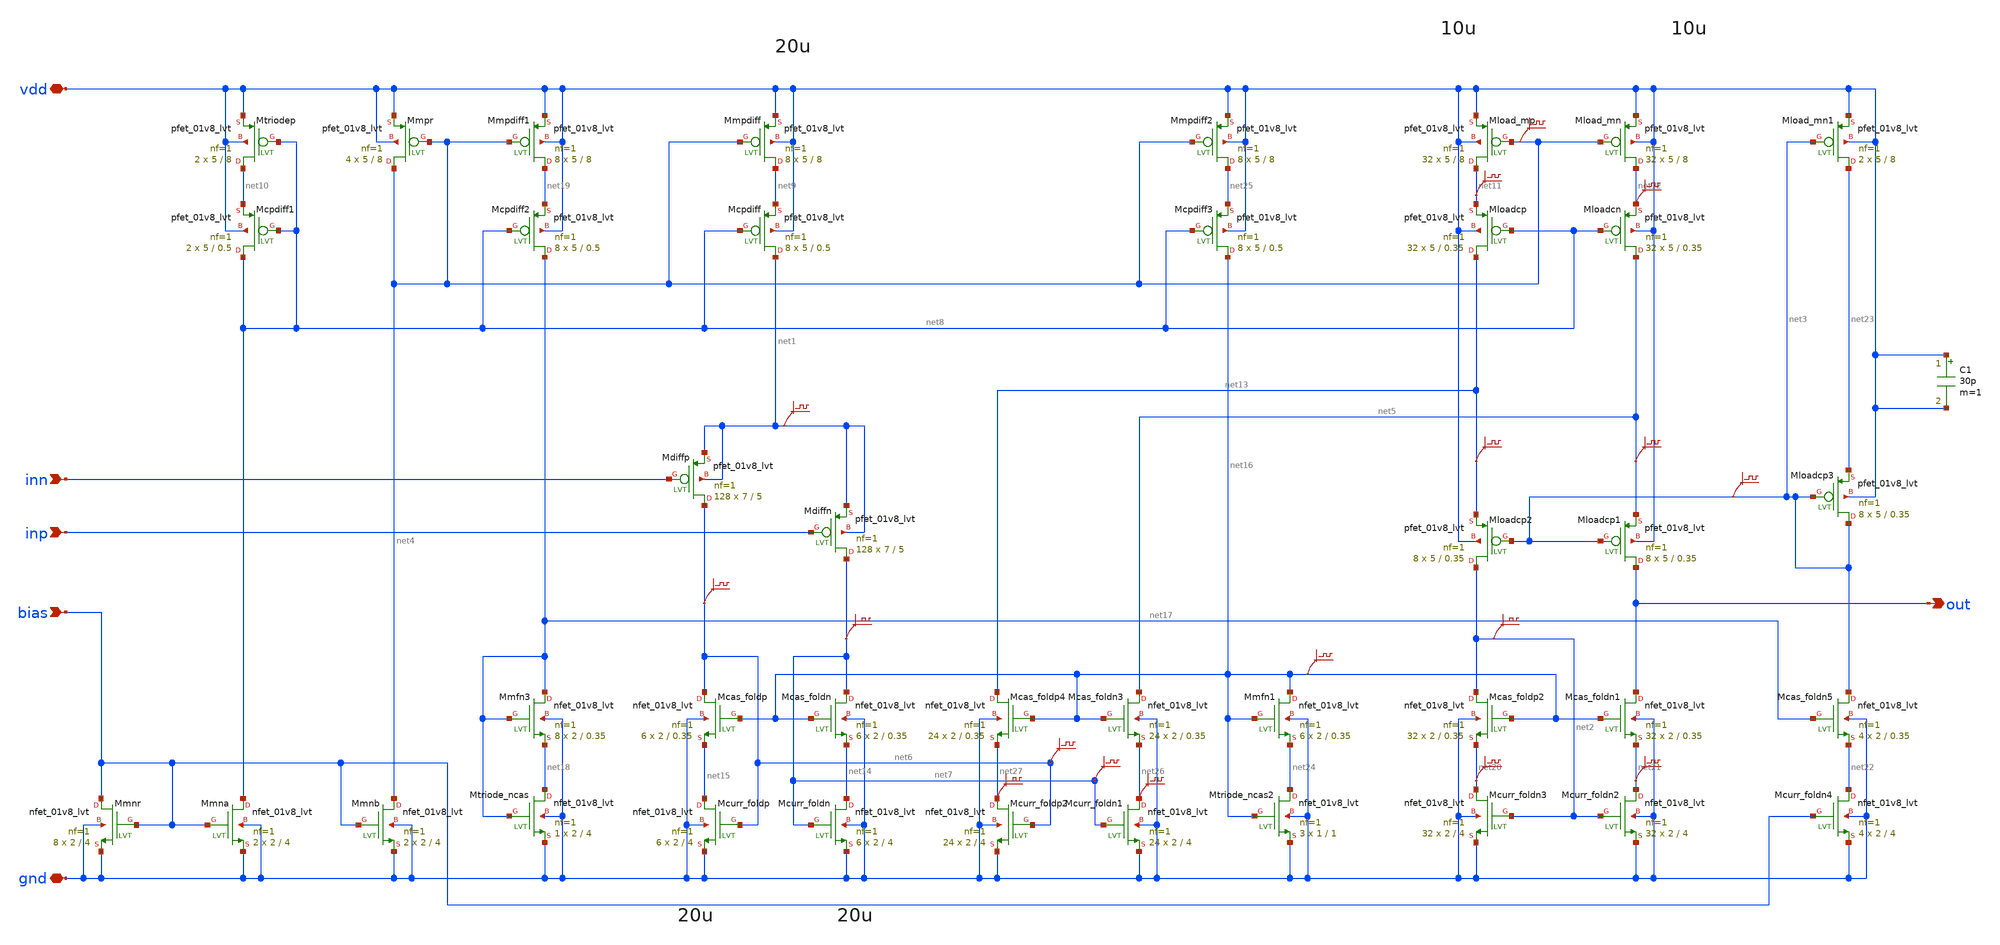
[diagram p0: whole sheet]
** sch_path: design/bandgap_opamp_doublefold/bandgap_opamp_doublefold.sch
**.subckt bandgap_opamp_doublefold inp inn bias out vdd gnd
*.ipin inp
*.ipin inn
*.ipin bias
*.opin out
*.iopin vdd
*.iopin gnd
XMmpdiff net9 net4 vdd vdd sky130_fd_pr__pfet_01v8_lvt L=8 W=5 nf=1 ad='W * 0.29' as='W * 0.29' pd='2 * (W + 0.29)'
+ ps='2 * (W + 0.29)' nrd='0.29 / W' nrs='0.29 / W' sa=0 sb=0 sd=0 mult=8 m=8
XMmpr net4 net4 vdd vdd sky130_fd_pr__pfet_01v8_lvt L=8 W=5 nf=1 ad='W * 0.29' as='W * 0.29' pd='2 * (W + 0.29)'
+ ps='2 * (W + 0.29)' nrd='0.29 / W' nrs='0.29 / W' sa=0 sb=0 sd=0 mult=4 m=4
XMmnr bias bias gnd gnd sky130_fd_pr__nfet_01v8_lvt L=4 W=2 nf=1 ad='W * 0.29' as='W * 0.29' pd='2 * (W + 0.29)'
+ ps='2 * (W + 0.29)' nrd='0.29 / W' nrs='0.29 / W' sa=0 sb=0 sd=0 mult=8 m=8
XMmnb net4 bias gnd gnd sky130_fd_pr__nfet_01v8_lvt L=4 W=2 nf=1 ad='W * 0.29' as='W * 0.29' pd='2 * (W + 0.29)'
+ ps='2 * (W + 0.29)' nrd='0.29 / W' nrs='0.29 / W' sa=0 sb=0 sd=0 mult=2 m=2
XMcpdiff net1 net8 net9 vdd sky130_fd_pr__pfet_01v8_lvt L=0.5 W=5 nf=1 ad='W * 0.29' as='W * 0.29' pd='2 * (W + 0.29)'
+ ps='2 * (W + 0.29)' nrd='0.29 / W' nrs='0.29 / W' sa=0 sb=0 sd=0 mult=8 m=8
XMmna net8 bias gnd gnd sky130_fd_pr__nfet_01v8_lvt L=4 W=2 nf=1 ad='W * 0.29' as='W * 0.29' pd='2 * (W + 0.29)'
+ ps='2 * (W + 0.29)' nrd='0.29 / W' nrs='0.29 / W' sa=0 sb=0 sd=0 mult=2 m=2
XMtriodep net10 net8 vdd vdd sky130_fd_pr__pfet_01v8_lvt L=8 W=5 nf=1 ad='W * 0.29' as='W * 0.29' pd='2 * (W + 0.29)'
+ ps='2 * (W + 0.29)' nrd='0.29 / W' nrs='0.29 / W' sa=0 sb=0 sd=0 mult=2 m=2
.save v(net6)
XMload_mp net11 net4 vdd vdd sky130_fd_pr__pfet_01v8_lvt L=8 W=5 nf=1 ad='W * 0.29' as='W * 0.29' pd='2 * (W + 0.29)'
+ ps='2 * (W + 0.29)' nrd='0.29 / W' nrs='0.29 / W' sa=0 sb=0 sd=0 mult=32 m=32
XMload_mn net12 net4 vdd vdd sky130_fd_pr__pfet_01v8_lvt L=8 W=5 nf=1 ad='W * 0.29' as='W * 0.29' pd='2 * (W + 0.29)'
+ ps='2 * (W + 0.29)' nrd='0.29 / W' nrs='0.29 / W' sa=0 sb=0 sd=0 mult=32 m=32
XMloadcn net5 net8 net12 vdd sky130_fd_pr__pfet_01v8_lvt L=0.35 W=5 nf=1 ad='W * 0.29' as='W * 0.29'
+ pd='2 * (W + 0.29)' ps='2 * (W + 0.29)' nrd='0.29 / W' nrs='0.29 / W' sa=0 sb=0 sd=0 mult=32 m=32
XMloadcp net13 net8 net11 vdd sky130_fd_pr__pfet_01v8_lvt L=0.35 W=5 nf=1 ad='W * 0.29' as='W * 0.29'
+ pd='2 * (W + 0.29)' ps='2 * (W + 0.29)' nrd='0.29 / W' nrs='0.29 / W' sa=0 sb=0 sd=0 mult=32 m=32
XMcurr_foldn net14 net7 gnd gnd sky130_fd_pr__nfet_01v8_lvt L=4 W=2 nf=1 ad='W * 0.29' as='W * 0.29'
+ pd='2 * (W + 0.29)' ps='2 * (W + 0.29)' nrd='0.29 / W' nrs='0.29 / W' sa=0 sb=0 sd=0 mult=6 m=6
XMcurr_foldp net15 net6 gnd gnd sky130_fd_pr__nfet_01v8_lvt L=4 W=2 nf=1 ad='W * 0.29' as='W * 0.29'
+ pd='2 * (W + 0.29)' ps='2 * (W + 0.29)' nrd='0.29 / W' nrs='0.29 / W' sa=0 sb=0 sd=0 mult=6 m=6
XMdiffn net7 inp net1 net1 sky130_fd_pr__pfet_01v8_lvt L=5 W=7 nf=1 ad='W * 0.29' as='W * 0.29' pd='2 * (W + 0.29)'
+ ps='2 * (W + 0.29)' nrd='0.29 / W' nrs='0.29 / W' sa=0 sb=0 sd=0 mult=128 m=128
XMdiffp net6 inn net1 net1 sky130_fd_pr__pfet_01v8_lvt L=5 W=7 nf=1 ad='W * 0.29' as='W * 0.29' pd='2 * (W + 0.29)'
+ ps='2 * (W + 0.29)' nrd='0.29 / W' nrs='0.29 / W' sa=0 sb=0 sd=0 mult=128 m=128
.save v(net1)
.save v(net12)
.save v(net4)
XMcpdiff1 net8 net8 net10 vdd sky130_fd_pr__pfet_01v8_lvt L=0.5 W=5 nf=1 ad='W * 0.29' as='W * 0.29'
+ pd='2 * (W + 0.29)' ps='2 * (W + 0.29)' nrd='0.29 / W' nrs='0.29 / W' sa=0 sb=0 sd=0 mult=2 m=2
.save v(net7)
XMcas_foldn net7 net16 net14 gnd sky130_fd_pr__nfet_01v8_lvt L=0.35 W=2 nf=1 ad='W * 0.29' as='W * 0.29'
+ pd='2 * (W + 0.29)' ps='2 * (W + 0.29)' nrd='0.29 / W' nrs='0.29 / W' sa=0 sb=0 sd=0 mult=6 m=6
XMcas_foldp net6 net16 net15 gnd sky130_fd_pr__nfet_01v8_lvt L=0.35 W=2 nf=1 ad='W * 0.29' as='W * 0.29'
+ pd='2 * (W + 0.29)' ps='2 * (W + 0.29)' nrd='0.29 / W' nrs='0.29 / W' sa=0 sb=0 sd=0 mult=6 m=6
XMmfn3 net17 net17 net18 gnd sky130_fd_pr__nfet_01v8_lvt L=0.35 W=2 nf=1 ad='W * 0.29' as='W * 0.29'
+ pd='2 * (W + 0.29)' ps='2 * (W + 0.29)' nrd='0.29 / W' nrs='0.29 / W' sa=0 sb=0 sd=0 mult=8 m=8
XMtriode_ncas net18 net17 gnd gnd sky130_fd_pr__nfet_01v8_lvt L=4 W=2 nf=1 ad='W * 0.29' as='W * 0.29'
+ pd='2 * (W + 0.29)' ps='2 * (W + 0.29)' nrd='0.29 / W' nrs='0.29 / W' sa=0 sb=0 sd=0 mult=1 m=1
XMmpdiff1 net19 net4 vdd vdd sky130_fd_pr__pfet_01v8_lvt L=8 W=5 nf=1 ad='W * 0.29' as='W * 0.29' pd='2 * (W + 0.29)'
+ ps='2 * (W + 0.29)' nrd='0.29 / W' nrs='0.29 / W' sa=0 sb=0 sd=0 mult=8 m=8
XMcpdiff2 net17 net8 net19 vdd sky130_fd_pr__pfet_01v8_lvt L=0.5 W=5 nf=1 ad='W * 0.29' as='W * 0.29'
+ pd='2 * (W + 0.29)' ps='2 * (W + 0.29)' nrd='0.29 / W' nrs='0.29 / W' sa=0 sb=0 sd=0 mult=8 m=8
.save v(net13)
C1 vdd vdd 30p m=1
.save v(net11)
XMcurr_foldn1 net26 net7 gnd gnd sky130_fd_pr__nfet_01v8_lvt L=4 W=2 nf=1 ad='W * 0.29' as='W * 0.29'
+ pd='2 * (W + 0.29)' ps='2 * (W + 0.29)' nrd='0.29 / W' nrs='0.29 / W' sa=0 sb=0 sd=0 mult=24 m=24
XMcurr_foldp2 net27 net6 gnd gnd sky130_fd_pr__nfet_01v8_lvt L=4 W=2 nf=1 ad='W * 0.29' as='W * 0.29'
+ pd='2 * (W + 0.29)' ps='2 * (W + 0.29)' nrd='0.29 / W' nrs='0.29 / W' sa=0 sb=0 sd=0 mult=24 m=24
XMcas_foldn3 net5 net16 net26 gnd sky130_fd_pr__nfet_01v8_lvt L=0.35 W=2 nf=1 ad='W * 0.29' as='W * 0.29'
+ pd='2 * (W + 0.29)' ps='2 * (W + 0.29)' nrd='0.29 / W' nrs='0.29 / W' sa=0 sb=0 sd=0 mult=24 m=24
XMcas_foldp4 net13 net16 net27 gnd sky130_fd_pr__nfet_01v8_lvt L=0.35 W=2 nf=1 ad='W * 0.29' as='W * 0.29'
+ pd='2 * (W + 0.29)' ps='2 * (W + 0.29)' nrd='0.29 / W' nrs='0.29 / W' sa=0 sb=0 sd=0 mult=24 m=24
.save v(net26)
XMloadcp1 out net3 net5 vdd sky130_fd_pr__pfet_01v8_lvt L=0.35 W=5 nf=1 ad='W * 0.29' as='W * 0.29' pd='2 * (W + 0.29)'
+ ps='2 * (W + 0.29)' nrd='0.29 / W' nrs='0.29 / W' sa=0 sb=0 sd=0 mult=8 m=8
XMloadcp2 net2 net3 net13 vdd sky130_fd_pr__pfet_01v8_lvt L=0.35 W=5 nf=1 ad='W * 0.29' as='W * 0.29'
+ pd='2 * (W + 0.29)' ps='2 * (W + 0.29)' nrd='0.29 / W' nrs='0.29 / W' sa=0 sb=0 sd=0 mult=8 m=8
XMcurr_foldn2 net21 net2 gnd gnd sky130_fd_pr__nfet_01v8_lvt L=4 W=2 nf=1 ad='W * 0.29' as='W * 0.29'
+ pd='2 * (W + 0.29)' ps='2 * (W + 0.29)' nrd='0.29 / W' nrs='0.29 / W' sa=0 sb=0 sd=0 mult=32 m=32
XMcurr_foldn3 net20 net2 gnd gnd sky130_fd_pr__nfet_01v8_lvt L=4 W=2 nf=1 ad='W * 0.29' as='W * 0.29'
+ pd='2 * (W + 0.29)' ps='2 * (W + 0.29)' nrd='0.29 / W' nrs='0.29 / W' sa=0 sb=0 sd=0 mult=32 m=32
XMcas_foldn1 out net16 net21 gnd sky130_fd_pr__nfet_01v8_lvt L=0.35 W=2 nf=1 ad='W * 0.29' as='W * 0.29'
+ pd='2 * (W + 0.29)' ps='2 * (W + 0.29)' nrd='0.29 / W' nrs='0.29 / W' sa=0 sb=0 sd=0 mult=32 m=32
XMcas_foldp2 net2 net16 net20 gnd sky130_fd_pr__nfet_01v8_lvt L=0.35 W=2 nf=1 ad='W * 0.29' as='W * 0.29'
+ pd='2 * (W + 0.29)' ps='2 * (W + 0.29)' nrd='0.29 / W' nrs='0.29 / W' sa=0 sb=0 sd=0 mult=32 m=32
XMload_mn1 net23 net3 vdd vdd sky130_fd_pr__pfet_01v8_lvt L=8 W=5 nf=1 ad='W * 0.29' as='W * 0.29' pd='2 * (W + 0.29)'
+ ps='2 * (W + 0.29)' nrd='0.29 / W' nrs='0.29 / W' sa=0 sb=0 sd=0 mult=2 m=2
XMcurr_foldn4 net22 bias gnd gnd sky130_fd_pr__nfet_01v8_lvt L=4 W=2 nf=1 ad='W * 0.29' as='W * 0.29'
+ pd='2 * (W + 0.29)' ps='2 * (W + 0.29)' nrd='0.29 / W' nrs='0.29 / W' sa=0 sb=0 sd=0 mult=4 m=4
XMcas_foldn5 net3 net17 net22 gnd sky130_fd_pr__nfet_01v8_lvt L=0.35 W=2 nf=1 ad='W * 0.29' as='W * 0.29'
+ pd='2 * (W + 0.29)' ps='2 * (W + 0.29)' nrd='0.29 / W' nrs='0.29 / W' sa=0 sb=0 sd=0 mult=4 m=4
XMloadcp3 net3 net3 net23 vdd sky130_fd_pr__pfet_01v8_lvt L=0.35 W=5 nf=1 ad='W * 0.29' as='W * 0.29'
+ pd='2 * (W + 0.29)' ps='2 * (W + 0.29)' nrd='0.29 / W' nrs='0.29 / W' sa=0 sb=0 sd=0 mult=8 m=8
.save v(net5)
.save v(net3)
.save v(net2)
.save v(net7)
XMmfn1 net16 net16 net24 gnd sky130_fd_pr__nfet_01v8_lvt L=0.35 W=2 nf=1 ad='W * 0.29' as='W * 0.29'
+ pd='2 * (W + 0.29)' ps='2 * (W + 0.29)' nrd='0.29 / W' nrs='0.29 / W' sa=0 sb=0 sd=0 mult=6 m=6
XMtriode_ncas2 net24 net16 gnd gnd sky130_fd_pr__nfet_01v8_lvt L=1 W=1 nf=1 ad='W * 0.29' as='W * 0.29'
+ pd='2 * (W + 0.29)' ps='2 * (W + 0.29)' nrd='0.29 / W' nrs='0.29 / W' sa=0 sb=0 sd=0 mult=3 m=3
.save v(net16)
XMmpdiff2 net25 net4 vdd vdd sky130_fd_pr__pfet_01v8_lvt L=8 W=5 nf=1 ad='W * 0.29' as='W * 0.29' pd='2 * (W + 0.29)'
+ ps='2 * (W + 0.29)' nrd='0.29 / W' nrs='0.29 / W' sa=0 sb=0 sd=0 mult=8 m=8
XMcpdiff3 net16 net8 net25 vdd sky130_fd_pr__pfet_01v8_lvt L=0.5 W=5 nf=1 ad='W * 0.29' as='W * 0.29'
+ pd='2 * (W + 0.29)' ps='2 * (W + 0.29)' nrd='0.29 / W' nrs='0.29 / W' sa=0 sb=0 sd=0 mult=8 m=8
.save v(net6)
.save v(net20)
.save v(net21)
.save v(net27)
**.ends
.end
